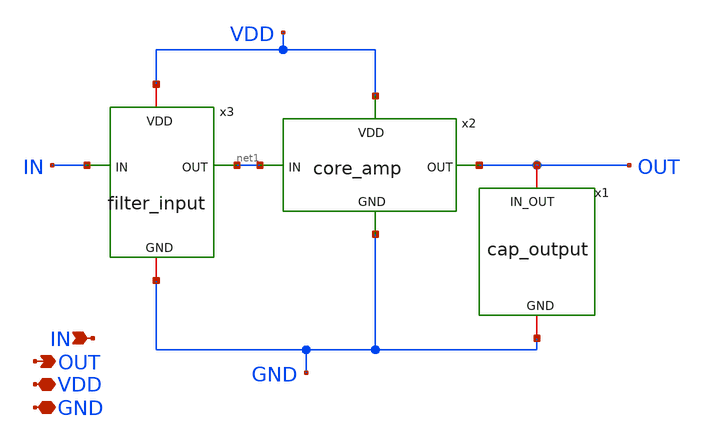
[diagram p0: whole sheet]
** sch_path: amp_top.sch
**.subckt amp_top IN OUT VDD GND
*.ipin IN
*.opin OUT
*.iopin VDD
*.iopin GND
x1 GND OUT cap_output
x3 IN net1 VDD GND filter_input
x2 net1 OUT VDD GND core_amp
**.ends
.end
